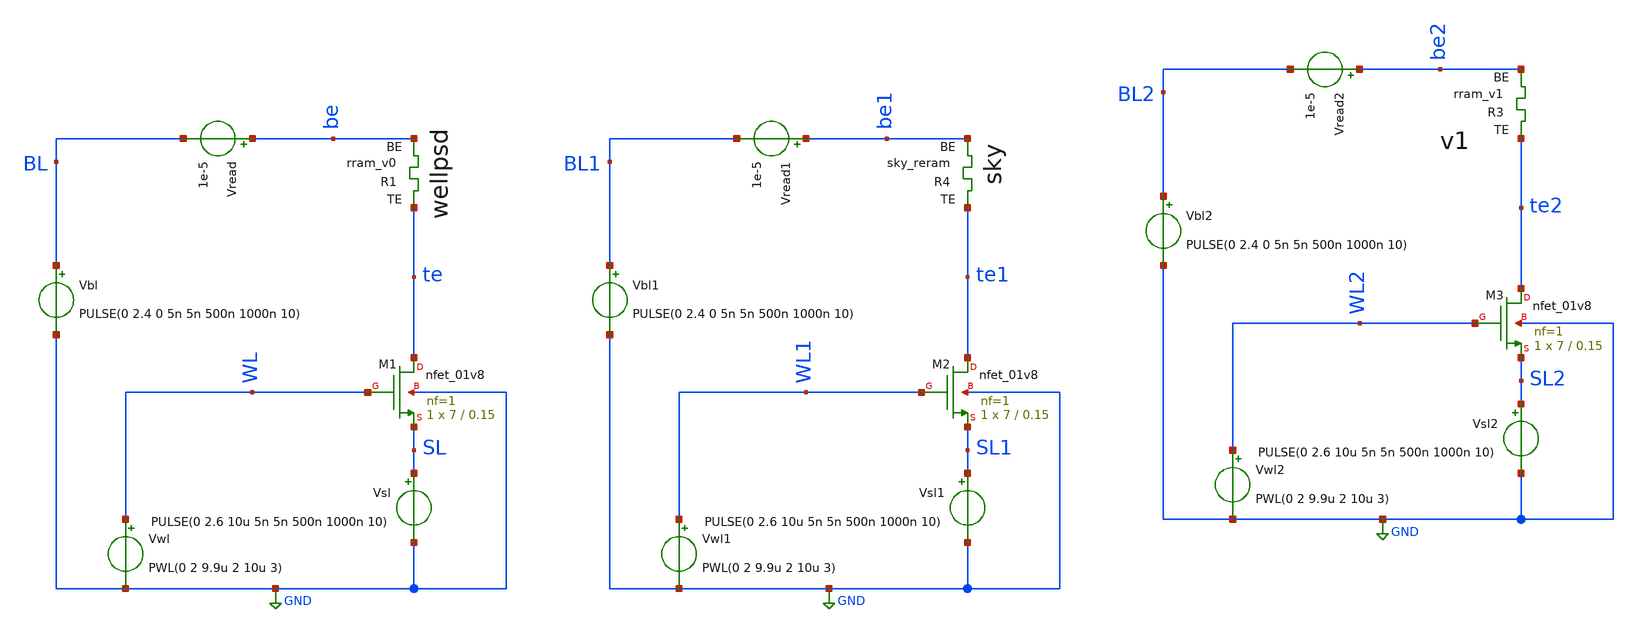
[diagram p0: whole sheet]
** sch_path: Memristor/tb_1T1R_pulses_rram_v0.sch
**.subckt tb_1T1R_pulses_rram_v0
XM1 te WL SL GND sky130_fd_pr__nfet_01v8 L=0.15 W=7 nf=1 ad='int((nf+1)/2) * W/nf * 0.29' as='int((nf+2)/2) * W/nf * 0.29'
+ pd='2*int((nf+1)/2) * (W/nf + 0.29)' ps='2*int((nf+2)/2) * (W/nf + 0.29)' nrd='0.29 / W' nrs='0.29 / W'
+ sa=0 sb=0 sd=0 mult=1 m=1
Vwl WL GND PWL(0 2 9.9u 2 10u 3)
Vbl BL GND PULSE(0 2.4 0 5n 5n 500n 1000n 10)
Vread be BL 1e-5
Vsl SL GND PULSE(0 2.6 10u 5n 5n 500n 1000n 10)
XR1 te be rram_v0
XM2 te1 WL1 SL1 GND sky130_fd_pr__nfet_01v8 L=0.15 W=7 nf=1 ad='int((nf+1)/2) * W/nf * 0.29' as='int((nf+2)/2) * W/nf * 0.29'
+ pd='2*int((nf+1)/2) * (W/nf + 0.29)' ps='2*int((nf+2)/2) * (W/nf + 0.29)' nrd='0.29 / W' nrs='0.29 / W'
+ sa=0 sb=0 sd=0 mult=1 m=1
Vwl1 WL1 GND PWL(0 2 9.9u 2 10u 3)
Vbl1 BL1 GND PULSE(0 2.4 0 5n 5n 500n 1000n 10)
Vread1 be1 BL1 1e-5
Vsl1 SL1 GND PULSE(0 2.6 10u 5n 5n 500n 1000n 10)
XR4 te1 be1 sky_reram
XM3 te2 WL2 SL2 GND sky130_fd_pr__nfet_01v8 L=0.15 W=7 nf=1 ad='int((nf+1)/2) * W/nf * 0.29' as='int((nf+2)/2) * W/nf * 0.29'
+ pd='2*int((nf+1)/2) * (W/nf + 0.29)' ps='2*int((nf+2)/2) * (W/nf + 0.29)' nrd='0.29 / W' nrs='0.29 / W'
+ sa=0 sb=0 sd=0 mult=1 m=1
Vwl2 WL2 GND PWL(0 2 9.9u 2 10u 3)
Vbl2 BL2 GND PULSE(0 2.4 0 5n 5n 500n 1000n 10)
Vread2 be2 BL2 1e-5
Vsl2 SL2 GND PULSE(0 2.6 10u 5n 5n 500n 1000n 10)
XR3 te2 be2 rram_v1
**** begin user architecture code


*.save @m.xm1.msky130_fd_pr__nfet_01v8[id]
.control
  * Modify according to your specific location
  save all
  tran 100n 20u
  write tb_1T1R_pulses_rram_v0.raw
.endc



.lib $::SKYWATER_MODELS/sky130.lib.spice tt

*MADE BY JORGE ALEJANDRO JUAREZ LORA IPN

.subckt rram_v0 TE BE
*N1 TE BE rram_v0_model gap_initial=unif(0.9,0.8)
N1 TE BE rram_v0_model
.ends rram_v0

.subckt rram_v1 TE BE
N1 TE BE rram_v1_model gap_initial=1.699
.ends rram_v0


.subckt sky_reram TE BE
N1 TE BE sky_reram_model
.ends sky_reram

.model rram_v0_model rram_v0_va
.model rram_v1_model rram_v1_va
.model sky_reram_model sky130_fd_pr_reram__reram_cell

.control
pre_osdi /foss/designs/SNN-MWIP/Memristor/rram_v0.osdi
pre_osdi /foss/designs/SNN-MWIP/Memristor/rram_v1.osdi
pre_osdi /foss/designs/SNN-MWIP/Memristor/sky.osdi
.endc

**** end user architecture code
**.ends
.GLOBAL GND
.end
